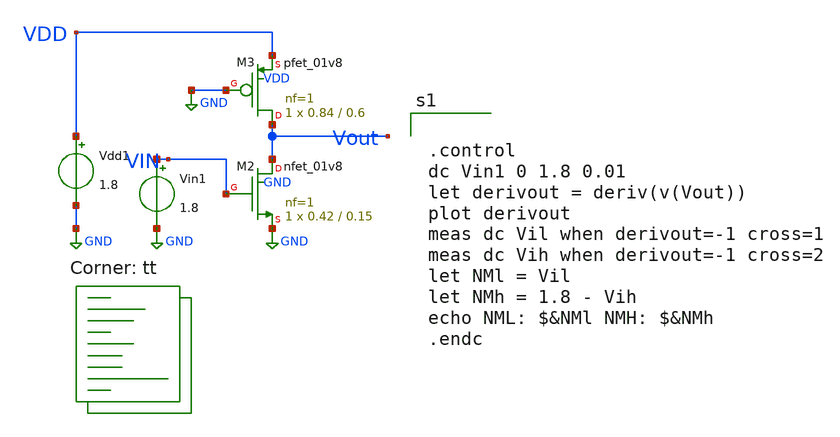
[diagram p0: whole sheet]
** sch_path: tutorial_3/tutorial_3_2b.sch
**.subckt tutorial_3_2b
XM2 Vout VIN GND GND sky130_fd_pr__nfet_01v8 L=0.15 W=0.42 nf=1 ad='int((nf+1)/2) * W/nf * 0.29' as='int((nf+2)/2) * W/nf * 0.29'
+ pd='2*int((nf+1)/2) * (W/nf + 0.29)' ps='2*int((nf+2)/2) * (W/nf + 0.29)' nrd='0.29 / W' nrs='0.29 / W'
+ sa=0 sb=0 sd=0 mult=1 m=1
XM3 Vout GND VDD VDD sky130_fd_pr__pfet_01v8 L=0.6 W=0.84 nf=1 ad='int((nf+1)/2) * W/nf * 0.29' as='int((nf+2)/2) * W/nf * 0.29'
+ pd='2*int((nf+1)/2) * (W/nf + 0.29)' ps='2*int((nf+2)/2) * (W/nf + 0.29)' nrd='0.29 / W' nrs='0.29 / W'
+ sa=0 sb=0 sd=0 mult=1 m=1
Vin1 VIN GND 1.8
Vdd1 VDD GND 1.8
**** begin user architecture code
.lib $::SKYWATER_MODELS/sky130.lib.spice tt


.control
dc Vin1 0 1.8 0.01
let derivout = deriv(v(Vout))
plot derivout
meas dc Vil when derivout=-1 cross=1
meas dc Vih when derivout=-1 cross=2
let NMl = Vil
let NMh = 1.8 - Vih
echo NML: $&NMl NMH: $&NMh
.endc

**** end user architecture code
**.ends
.GLOBAL GND
.end
